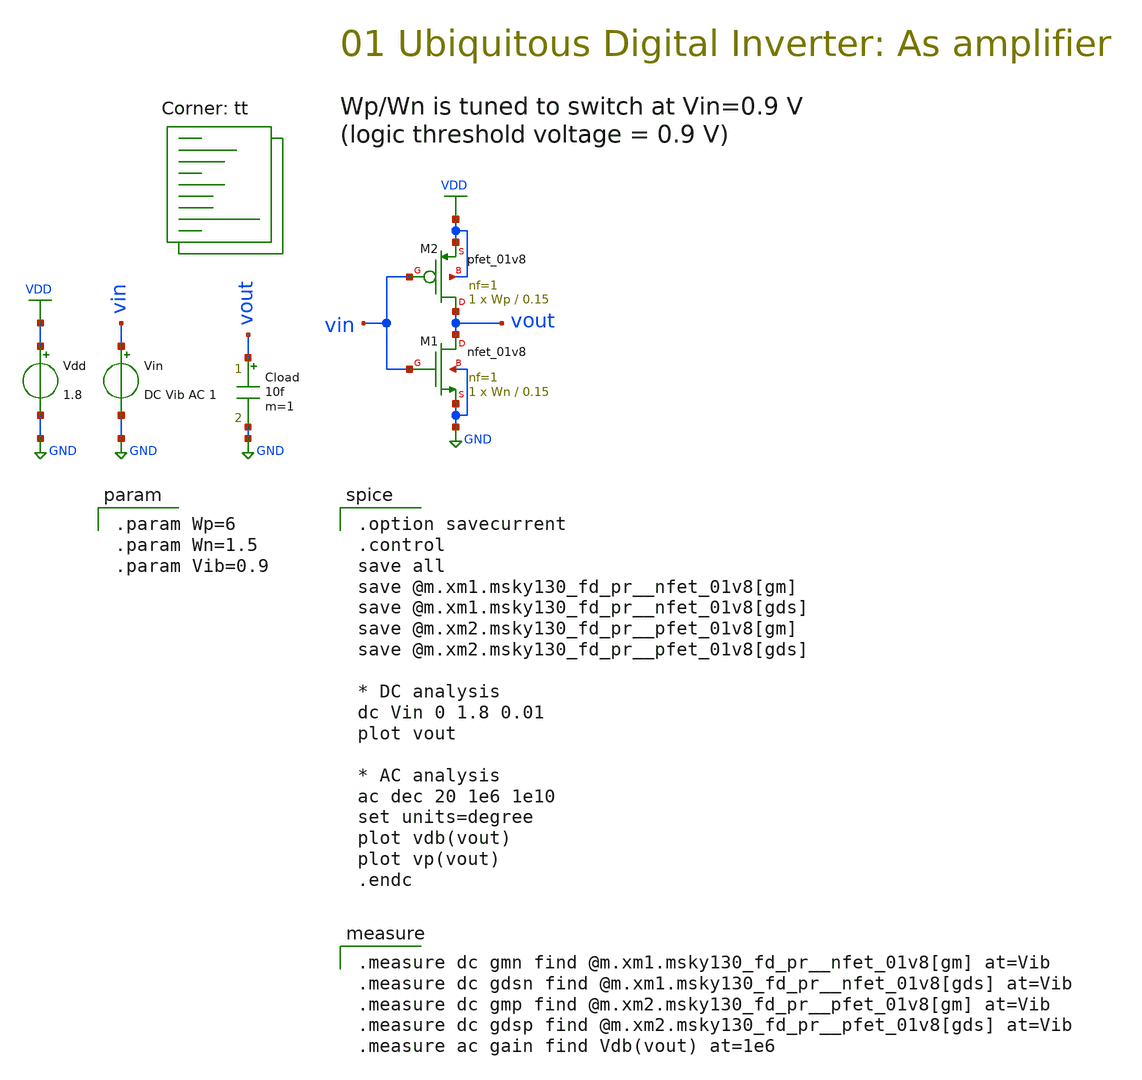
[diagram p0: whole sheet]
** sch_path: 01-c_inverter_amp.sch
**.subckt 01-c_inverter_amp
Vdd VDD GND 1.8
Vin vin GND DC Vib AC 1
XM2 vout vin VDD VDD sky130_fd_pr__pfet_01v8 L=0.15 W=Wp nf=1 ad='int((nf+1)/2) * W/nf * 0.29' as='int((nf+2)/2) * W/nf * 0.29'
+ pd='2*int((nf+1)/2) * (W/nf + 0.29)' ps='2*int((nf+2)/2) * (W/nf + 0.29)' nrd='0.29 / W' nrs='0.29 / W'
+ sa=0 sb=0 sd=0 mult=1 m=1
XM1 vout vin GND GND sky130_fd_pr__nfet_01v8 L=0.15 W=Wn nf=1 ad='int((1 + 1)/2) * Wn / 1 * 0.29' as='int((1 + 2)/2) * Wn / 1 * 0.29'
+ pd='2*int((1 + 1)/2) * (Wn / 1 + 0.29)' ps='2*int((1 + 2)/2) * (Wn / 1 + 0.29)' nrd='0.29 / Wn ' nrs='0.29 / Wn '
+ sa=0 sb=0 sd=0 mult=1 m=1
Cload vout GND 10f m=1
**** begin user architecture code
.lib $::SKYWATER_MODELS/sky130.lib.spice tt

.param Wp=6
.param Wn=1.5
.param Vib=0.9


.option savecurrent
.control
save all
save @m.xm1.msky130_fd_pr__nfet_01v8[gm]
save @m.xm1.msky130_fd_pr__nfet_01v8[gds]
save @m.xm2.msky130_fd_pr__pfet_01v8[gm]
save @m.xm2.msky130_fd_pr__pfet_01v8[gds]

* DC analysis
dc Vin 0 1.8 0.01
plot vout

* AC analysis
ac dec 20 1e6 1e10
set units=degree
plot vdb(vout)
plot vp(vout)
.endc


.measure dc gmn find @m.xm1.msky130_fd_pr__nfet_01v8[gm] at=Vib
.measure dc gdsn find @m.xm1.msky130_fd_pr__nfet_01v8[gds] at=Vib
.measure dc gmp find @m.xm2.msky130_fd_pr__pfet_01v8[gm] at=Vib
.measure dc gdsp find @m.xm2.msky130_fd_pr__pfet_01v8[gds] at=Vib
.measure ac gain find Vdb(vout) at=1e6

**** end user architecture code
**.ends
.GLOBAL GND
.GLOBAL VDD
.end
